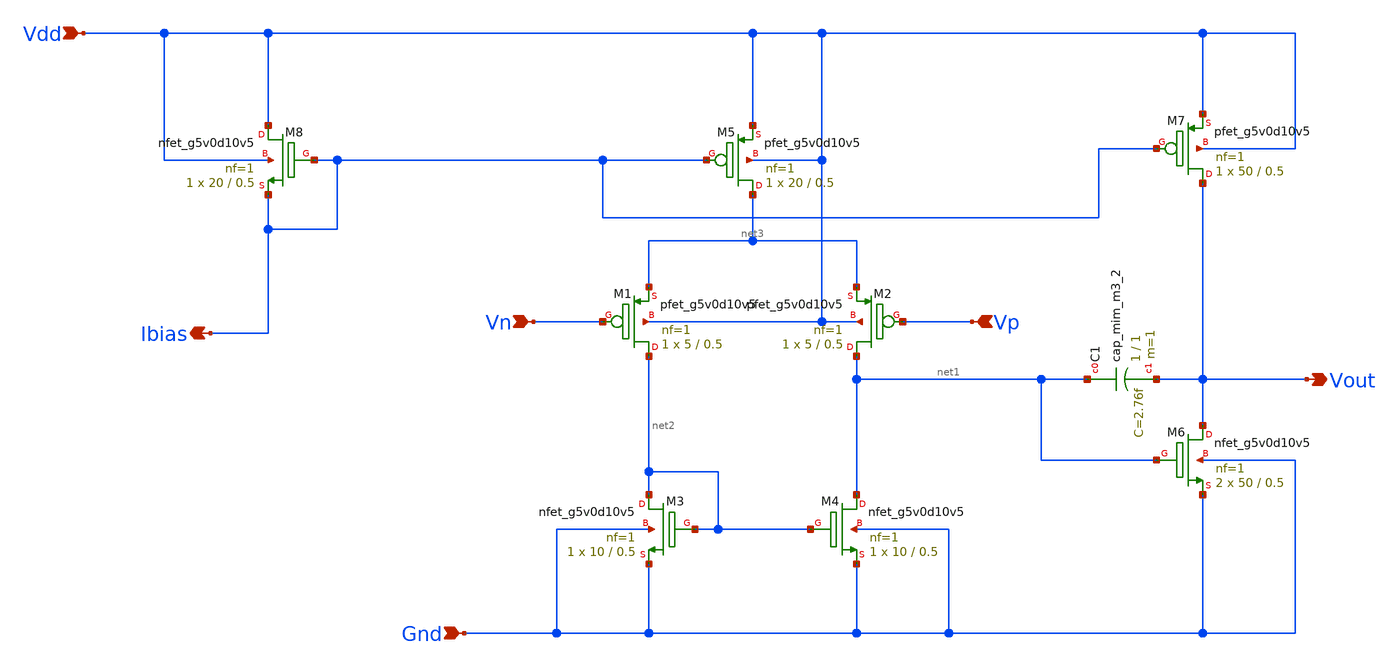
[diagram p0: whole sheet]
** sch_path: OTA/Schematic/Miller_OTA_PMOS.sch
**.subckt Miller_OTA_PMOS Vp Vn Ibias Vdd Gnd Vout
*.ipin Vp
*.ipin Vn
*.opin Ibias
*.ipin Vdd
*.ipin Gnd
*.opin Vout
XM5 net3 Ibias Vdd Vdd sky130_fd_pr__pfet_g5v0d10v5 L=0.5 W=20 nf=1 ad='int((nf+1)/2) * W/nf * 0.29'
+ as='int((nf+2)/2) * W/nf * 0.29' pd='2*int((nf+1)/2) * (W/nf + 0.29)' ps='2*int((nf+2)/2) * (W/nf + 0.29)'
+ nrd='0.29 / W' nrs='0.29 / W' sa=0 sb=0 sd=0 mult=1 m=1
XM7 Vout Ibias Vdd Vdd sky130_fd_pr__pfet_g5v0d10v5 L=0.5 W=50 nf=1 ad='int((nf+1)/2) * W/nf * 0.29'
+ as='int((nf+2)/2) * W/nf * 0.29' pd='2*int((nf+1)/2) * (W/nf + 0.29)' ps='2*int((nf+2)/2) * (W/nf + 0.29)'
+ nrd='0.29 / W' nrs='0.29 / W' sa=0 sb=0 sd=0 mult=1 m=1
XC1 net1 Vout sky130_fd_pr__cap_mim_m3_2 W=1 L=1 MF=1 m=1
XM1 net2 Vn net3 Vdd sky130_fd_pr__pfet_g5v0d10v5 L=0.5 W=5 nf=1 ad='int((nf+1)/2) * W/nf * 0.29' as='int((nf+2)/2) * W/nf * 0.29'
+ pd='2*int((nf+1)/2) * (W/nf + 0.29)' ps='2*int((nf+2)/2) * (W/nf + 0.29)' nrd='0.29 / W' nrs='0.29 / W'
+ sa=0 sb=0 sd=0 mult=1 m=1
XM8 Vdd Ibias Ibias Vdd sky130_fd_pr__nfet_g5v0d10v5 L=0.5 W=20 nf=1 ad='int((nf+1)/2) * W/nf * 0.29'
+ as='int((nf+2)/2) * W/nf * 0.29' pd='2*int((nf+1)/2) * (W/nf + 0.29)' ps='2*int((nf+2)/2) * (W/nf + 0.29)'
+ nrd='0.29 / W' nrs='0.29 / W' sa=0 sb=0 sd=0 mult=1 m=1
XM3 net2 net2 Gnd Gnd sky130_fd_pr__nfet_g5v0d10v5 L=0.5 W=10 nf=1 ad='int((nf+1)/2) * W/nf * 0.29' as='int((nf+2)/2) * W/nf * 0.29'
+ pd='2*int((nf+1)/2) * (W/nf + 0.29)' ps='2*int((nf+2)/2) * (W/nf + 0.29)' nrd='0.29 / W' nrs='0.29 / W'
+ sa=0 sb=0 sd=0 mult=1 m=1
XM2 net1 Vp net3 Vdd sky130_fd_pr__pfet_g5v0d10v5 L=0.5 W=5 nf=1 ad='int((nf+1)/2) * W/nf * 0.29' as='int((nf+2)/2) * W/nf * 0.29'
+ pd='2*int((nf+1)/2) * (W/nf + 0.29)' ps='2*int((nf+2)/2) * (W/nf + 0.29)' nrd='0.29 / W' nrs='0.29 / W'
+ sa=0 sb=0 sd=0 mult=1 m=1
XM4 net1 net2 Gnd Gnd sky130_fd_pr__nfet_g5v0d10v5 L=0.5 W=10 nf=1 ad='int((nf+1)/2) * W/nf * 0.29' as='int((nf+2)/2) * W/nf * 0.29'
+ pd='2*int((nf+1)/2) * (W/nf + 0.29)' ps='2*int((nf+2)/2) * (W/nf + 0.29)' nrd='0.29 / W' nrs='0.29 / W'
+ sa=0 sb=0 sd=0 mult=1 m=1
XM6 Vout net1 Gnd Gnd sky130_fd_pr__nfet_g5v0d10v5 L=0.5 W=50 nf=1 ad='int((nf+1)/2) * W/nf * 0.29' as='int((nf+2)/2) * W/nf * 0.29'
+ pd='2*int((nf+1)/2) * (W/nf + 0.29)' ps='2*int((nf+2)/2) * (W/nf + 0.29)' nrd='0.29 / W' nrs='0.29 / W'
+ sa=0 sb=0 sd=0 mult=2 m=2
**.ends
.end
